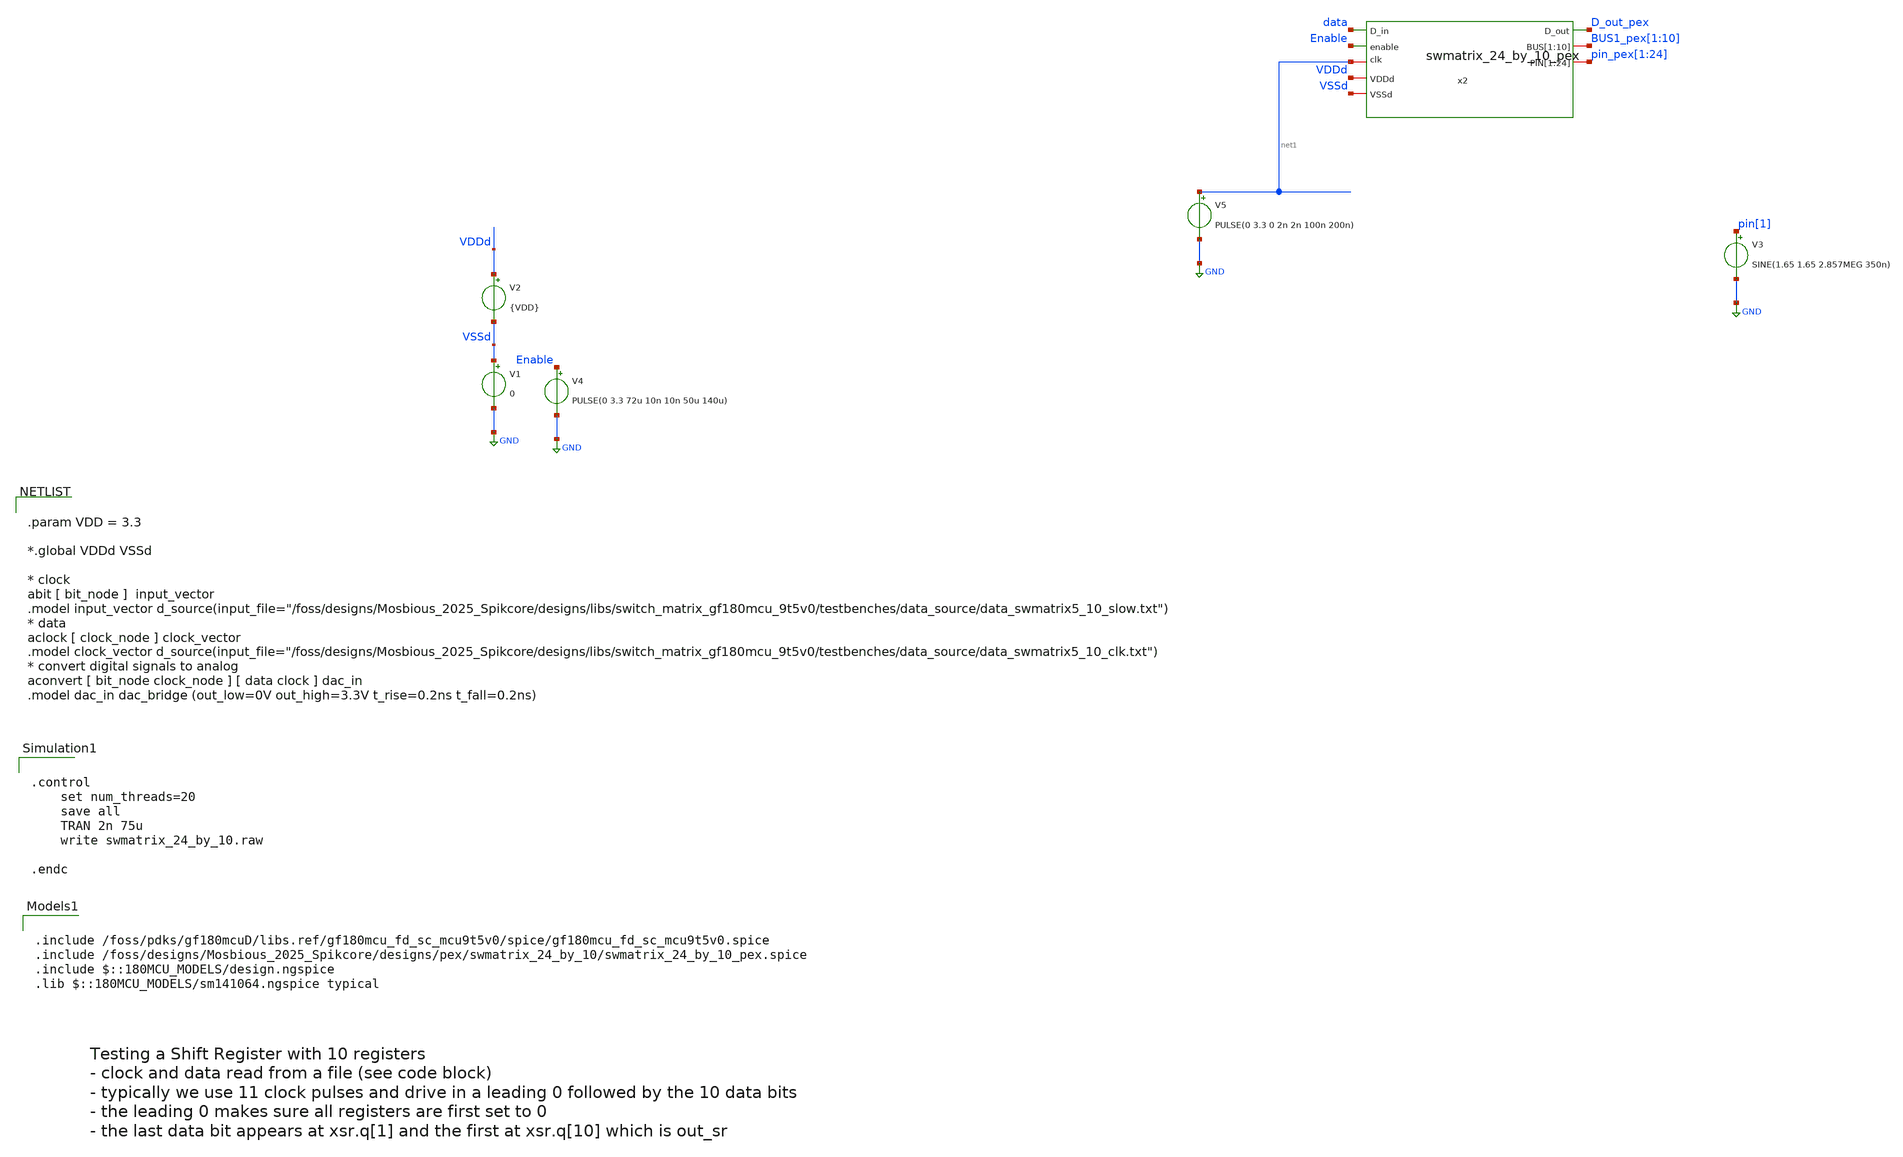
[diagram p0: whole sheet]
** sch_path: designs/pex/swmatrix_24_by_10/swmatrix_24_by_10_pex.sch
**.subckt swmatrix_24_by_10_pex
V1 VSSd GND 0
V2 VDDd VSSd {VDD}
V3 pin[1] GND SINE(1.65 1.65 2.857MEG 350n)
V4 Enable GND PULSE(0 3.3 72u 10n 10n 50u 140u)
V5 net1 GND PULSE(0 3.3 0 2n 2n 100n 200n)
x2 D_out_pex BUS1_pex[1] BUS1_pex[2] BUS1_pex[3] BUS1_pex[4] BUS1_pex[5] BUS1_pex[6] BUS1_pex[7]
+ BUS1_pex[8] BUS1_pex[9] BUS1_pex[10] pin_pex[1] pin_pex[2] pin_pex[3] pin_pex[4] pin_pex[5] pin_pex[6]
+ pin_pex[7] pin_pex[8] pin_pex[9] pin_pex[10] pin_pex[11] pin_pex[12] pin_pex[13] pin_pex[14] pin_pex[15]
+ pin_pex[16] pin_pex[17] pin_pex[18] pin_pex[19] pin_pex[20] pin_pex[21] pin_pex[22] pin_pex[23] pin_pex[24]
+ data VDDd Enable VSSd net1 swmatrix_24_by_10_pex
**** begin user architecture code


.param VDD = 3.3

*.global VDDd VSSd

* clock
abit [ bit_node ]  input_vector
.model input_vector
+ d_source(input_file="/foss/designs/Mosbious_2025_Spikcore/designs/libs/switch_matrix_gf180mcu_9t5v0/testbenches/data_source/data_swmatrix5_10_slow.txt")
* data
aclock [ clock_node ] clock_vector
.model clock_vector
+ d_source(input_file="/foss/designs/Mosbious_2025_Spikcore/designs/libs/switch_matrix_gf180mcu_9t5v0/testbenches/data_source/data_swmatrix5_10_clk.txt")
* convert digital signals to analog
aconvert [ bit_node clock_node ] [ data clock ] dac_in
.model dac_in dac_bridge (out_low=0V out_high=3.3V t_rise=0.2ns t_fall=0.2ns)




.control
    set num_threads=20
    save all
    TRAN 2n 75u
    write swmatrix_24_by_10.raw

.endc



.include /foss/pdks/gf180mcuD/libs.ref/gf180mcu_fd_sc_mcu9t5v0/spice/gf180mcu_fd_sc_mcu9t5v0.spice
.include /foss/designs/Mosbious_2025_Spikcore/designs/pex/swmatrix_24_by_10/swmatrix_24_by_10_pex.spice
.include $::180MCU_MODELS/design.ngspice
.lib $::180MCU_MODELS/sm141064.ngspice typical

**** end user architecture code
**.ends
.GLOBAL GND
.end
